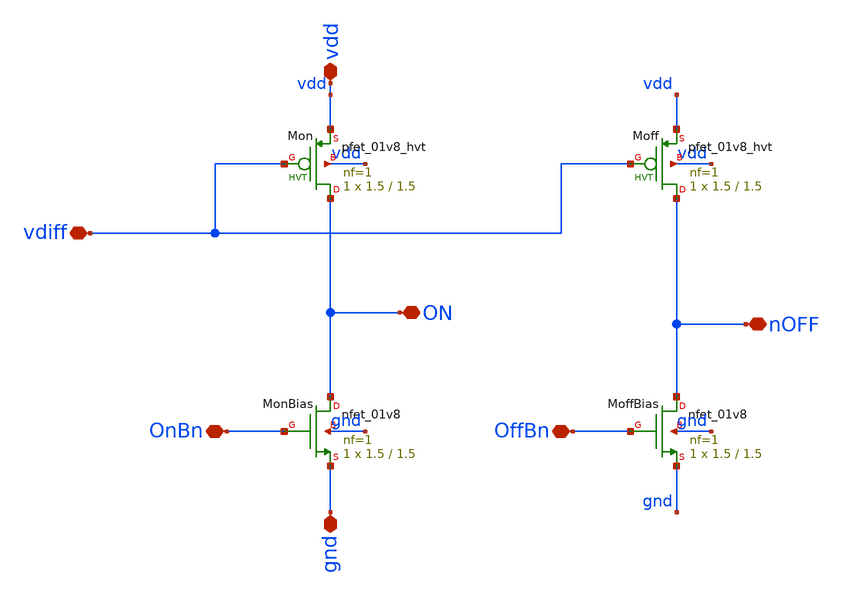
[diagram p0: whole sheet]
** sch_path: analog/xschem/PixelComparators.sch
**.subckt PixelComparators OnBn OffBn vdd vdiff gnd ON nOFF
*.iopin OnBn
*.iopin OffBn
*.iopin vdd
*.iopin vdiff
*.iopin gnd
*.iopin ON
*.iopin nOFF
XMonBias ON OnBn gnd gnd sky130_fd_pr__nfet_01v8 L=1.5 W=1.5 nf=1 ad='int((1 + 1)/2) * 1.5 / 1 * 0.29'
+ as='int((1 + 2)/2) * 1.5 / 1 * 0.29' pd='2*int((1 + 1)/2) * (1.5 / 1 + 0.29)' ps='2*int((1 + 2)/2) * (1.5 / 1 + 0.29)'
+ nrd='0.29 / 1.5 ' nrs='0.29 / 1.5 ' sa=0 sb=0 sd=0 mult=1 m=1
XMoffBias nOFF OffBn gnd gnd sky130_fd_pr__nfet_01v8 L=1.5 W=1.5 nf=1 ad='int((1 + 1)/2) * 1.5 / 1 * 0.29'
+ as='int((1 + 2)/2) * 1.5 / 1 * 0.29' pd='2*int((1 + 1)/2) * (1.5 / 1 + 0.29)' ps='2*int((1 + 2)/2) * (1.5 / 1 + 0.29)'
+ nrd='0.29 / 1.5 ' nrs='0.29 / 1.5 ' sa=0 sb=0 sd=0 mult=1 m=1
XMon ON vdiff vdd vdd sky130_fd_pr__pfet_01v8_hvt L=1.5 W=1.5 nf=1 ad='int((1 + 1)/2) * 1.5 / 1 * 0.29'
+ as='int((1 + 2)/2) * 1.5 / 1 * 0.29' pd='2*int((1 + 1)/2) * (1.5 / 1 + 0.29)' ps='2*int((1 + 2)/2) * (1.5 / 1 + 0.29)'
+ nrd='0.29 / 1.5 ' nrs='0.29 / 1.5 ' sa=0 sb=0 sd=0 mult=1 m=1
XMoff nOFF vdiff vdd vdd sky130_fd_pr__pfet_01v8_hvt L=1.5 W=1.5 nf=1 ad='int((1 + 1)/2) * 1.5 / 1 * 0.29'
+ as='int((1 + 2)/2) * 1.5 / 1 * 0.29' pd='2*int((1 + 1)/2) * (1.5 / 1 + 0.29)' ps='2*int((1 + 2)/2) * (1.5 / 1 + 0.29)'
+ nrd='0.29 / 1.5 ' nrs='0.29 / 1.5 ' sa=0 sb=0 sd=0 mult=1 m=1
**.ends
.end
